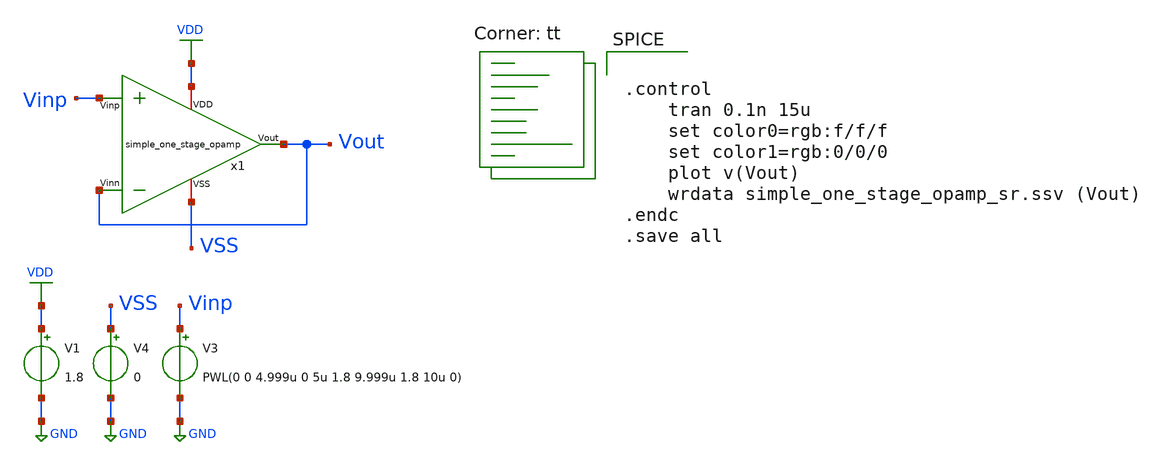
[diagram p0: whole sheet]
** sch_path: opamp_design/cascode_one_stage_opamp/simple_one_stage_opamp_sr.sch
**.subckt simple_one_stage_opamp_sr
V1 VDD GND 1.8
V3 Vinp GND PWL(0 0 4.999u 0 5u 1.8 9.999u 1.8 10u 0)
V4 VSS GND 0
x1 VDD Vout Vinp Vout VSS simple_one_stage_opamp
**** begin user architecture code


.control
	tran 0.1n 15u
	set color0=rgb:f/f/f
	set color1=rgb:0/0/0
	plot v(Vout)
	wrdata simple_one_stage_opamp_sr.ssv (Vout)
.endc
.save all


.lib $::SKYWATER_MODELS/sky130.lib.spice tt
**** end user architecture code
**.ends

* expanding   symbol:
*+  /home/ricardo/RATT_repos/Proyectos_xschem/opamp_design/simple_one_stage_opamp/simple_one_stage_opamp.sym # of pins=5
** sym_path: opamp_design/simple_one_stage_opamp/simple_one_stage_opamp.sym
** sch_path: opamp_design/simple_one_stage_opamp/simple_one_stage_opamp.sch
.subckt simple_one_stage_opamp VDD Vout Vinp Vinn VSS
*.iopin VSS
*.iopin VDD
*.ipin Vinp
*.ipin Vinn
*.opin Vout
XM1 net2 Vinp net1 VSS sky130_fd_pr__nfet_01v8 L=0.15 W=15.648 nf=1 ad='int((nf+1)/2) * W/nf * 0.29'
+ as='int((nf+2)/2) * W/nf * 0.29' pd='2*int((nf+1)/2) * (W/nf + 0.29)' ps='2*int((nf+2)/2) * (W/nf + 0.29)'
+ nrd='0.29 / W' nrs='0.29 / W' sa=0 sb=0 sd=0 mult=1 m=1
XM4 net2 net2 VDD VDD sky130_fd_pr__pfet_01v8 L=0.15 W=0.449 nf=1 ad='int((nf+1)/2) * W/nf * 0.29' as='int((nf+2)/2) * W/nf * 0.29'
+ pd='2*int((nf+1)/2) * (W/nf + 0.29)' ps='2*int((nf+2)/2) * (W/nf + 0.29)' nrd='0.29 / W' nrs='0.29 / W'
+ sa=0 sb=0 sd=0 mult=1 m=1
XM2 Vout Vinn net1 VSS sky130_fd_pr__nfet_01v8 L=0.15 W=15.648 nf=1 ad='int((nf+1)/2) * W/nf * 0.29'
+ as='int((nf+2)/2) * W/nf * 0.29' pd='2*int((nf+1)/2) * (W/nf + 0.29)' ps='2*int((nf+2)/2) * (W/nf + 0.29)'
+ nrd='0.29 / W' nrs='0.29 / W' sa=0 sb=0 sd=0 mult=1 m=1
XM3 Vout net2 VDD VDD sky130_fd_pr__pfet_01v8 L=0.15 W=0.449 nf=1 ad='int((nf+1)/2) * W/nf * 0.29' as='int((nf+2)/2) * W/nf * 0.29'
+ pd='2*int((nf+1)/2) * (W/nf + 0.29)' ps='2*int((nf+2)/2) * (W/nf + 0.29)' nrd='0.29 / W' nrs='0.29 / W'
+ sa=0 sb=0 sd=0 mult=1 m=1
XM5 net1 net3 VSS VSS sky130_fd_pr__nfet_01v8 L=0.15 W=5.193 nf=1 ad='int((nf+1)/2) * W/nf * 0.29' as='int((nf+2)/2) * W/nf * 0.29'
+ pd='2*int((nf+1)/2) * (W/nf + 0.29)' ps='2*int((nf+2)/2) * (W/nf + 0.29)' nrd='0.29 / W' nrs='0.29 / W'
+ sa=0 sb=0 sd=0 mult=1 m=1
XM6 net3 net3 VSS VSS sky130_fd_pr__nfet_01v8 L=0.15 W=5.193 nf=1 ad='int((nf+1)/2) * W/nf * 0.29' as='int((nf+2)/2) * W/nf * 0.29'
+ pd='2*int((nf+1)/2) * (W/nf + 0.29)' ps='2*int((nf+2)/2) * (W/nf + 0.29)' nrd='0.29 / W' nrs='0.29 / W'
+ sa=0 sb=0 sd=0 mult=1 m=1
I0 VDD net3 48u
.ends

.GLOBAL VDD
.GLOBAL GND
.end
